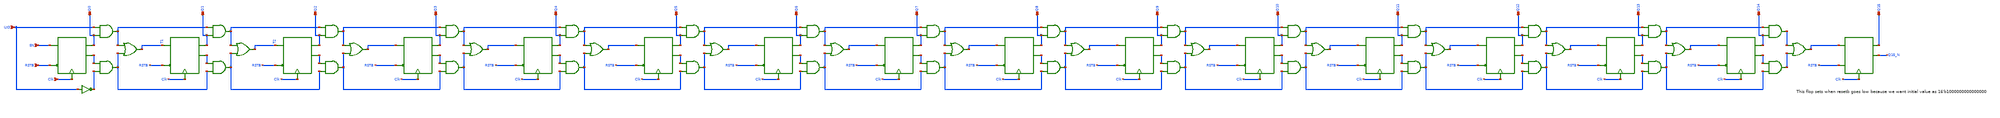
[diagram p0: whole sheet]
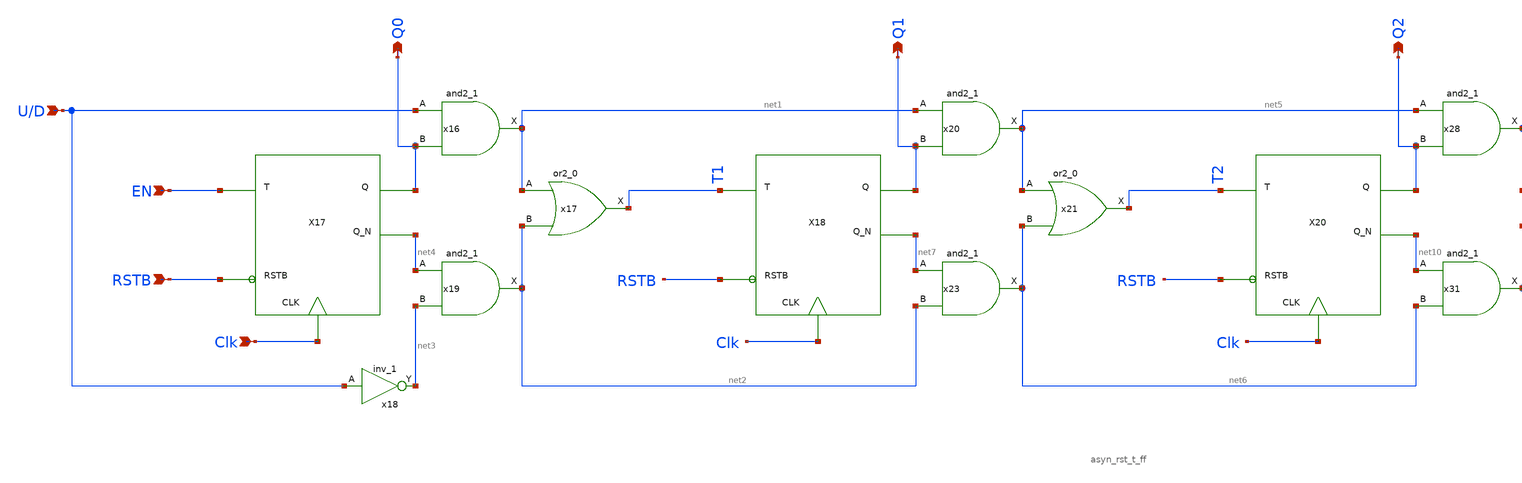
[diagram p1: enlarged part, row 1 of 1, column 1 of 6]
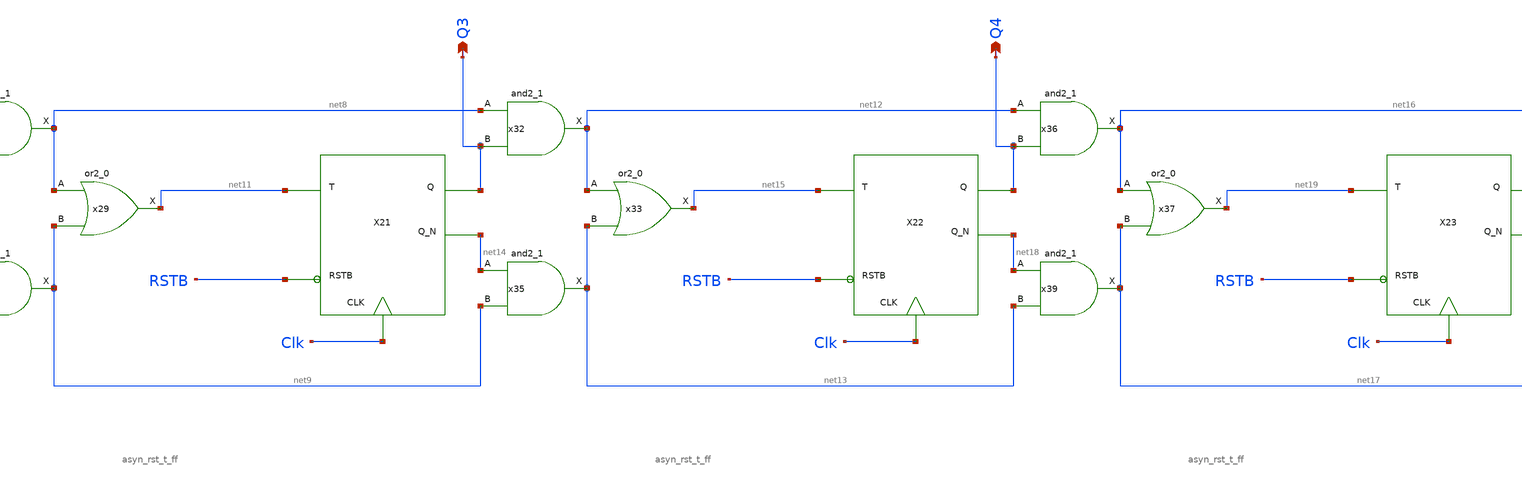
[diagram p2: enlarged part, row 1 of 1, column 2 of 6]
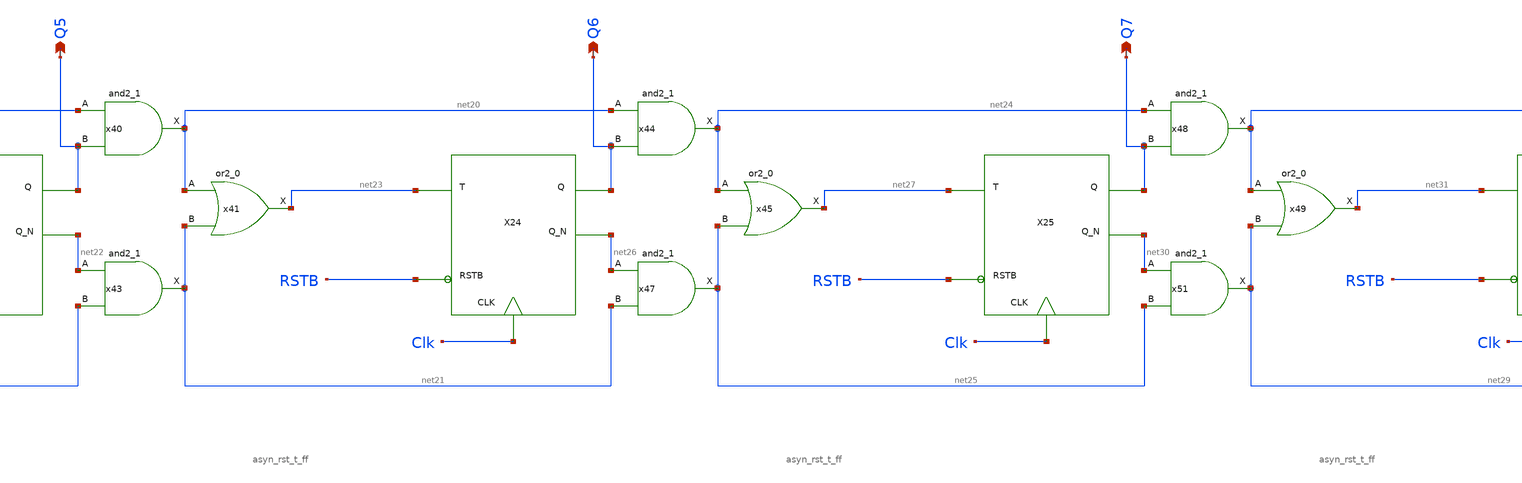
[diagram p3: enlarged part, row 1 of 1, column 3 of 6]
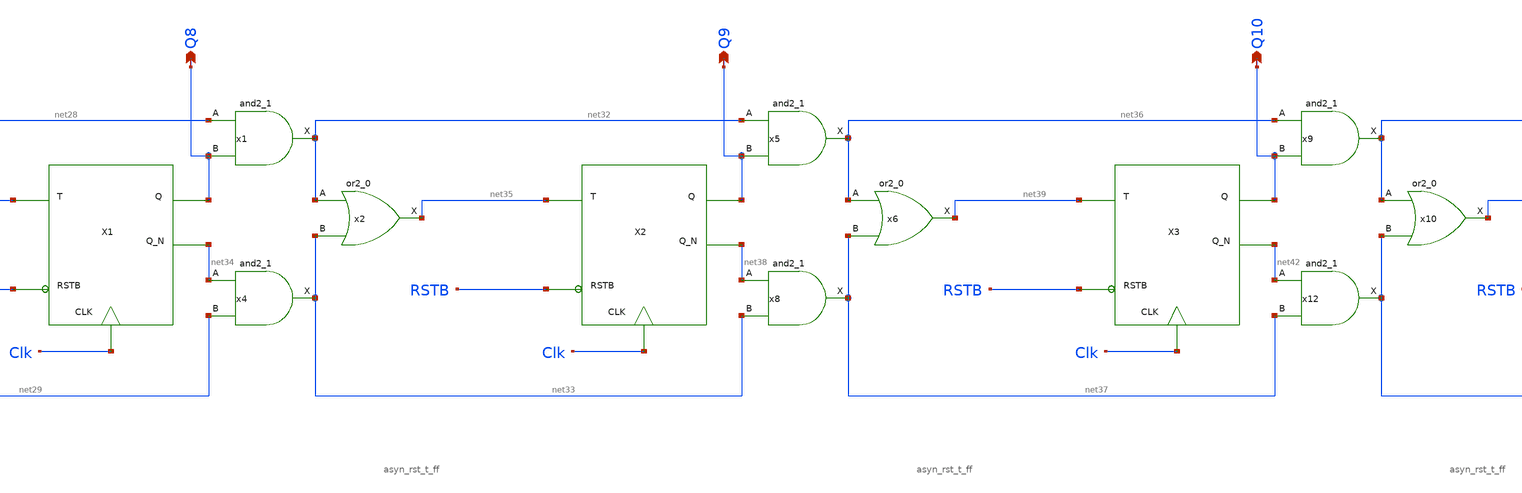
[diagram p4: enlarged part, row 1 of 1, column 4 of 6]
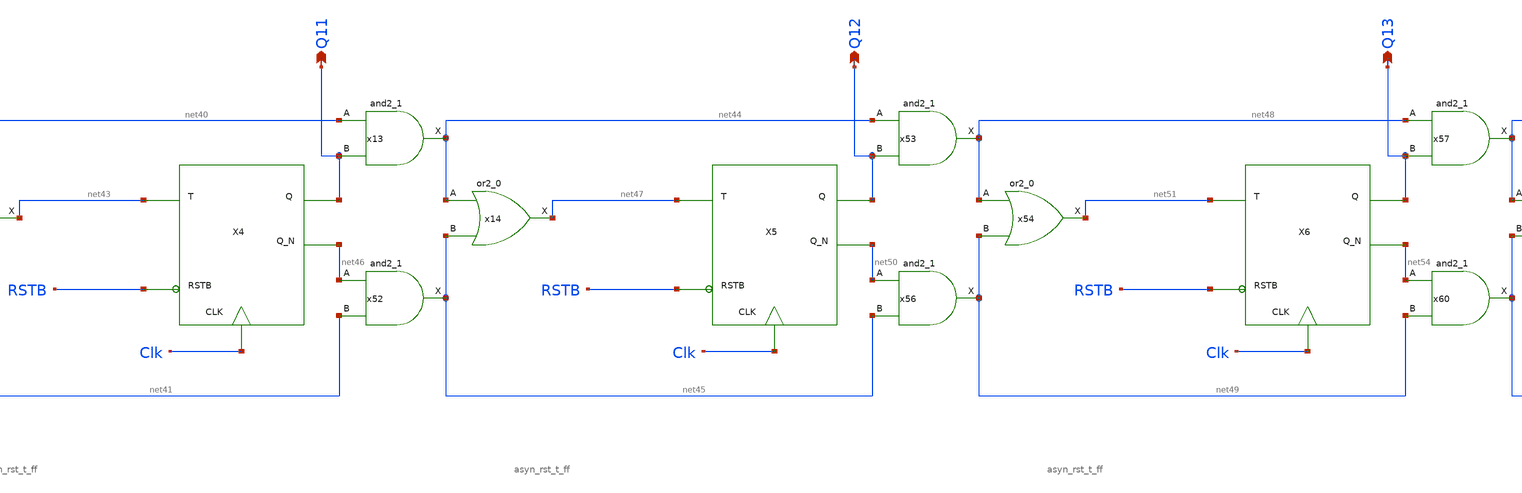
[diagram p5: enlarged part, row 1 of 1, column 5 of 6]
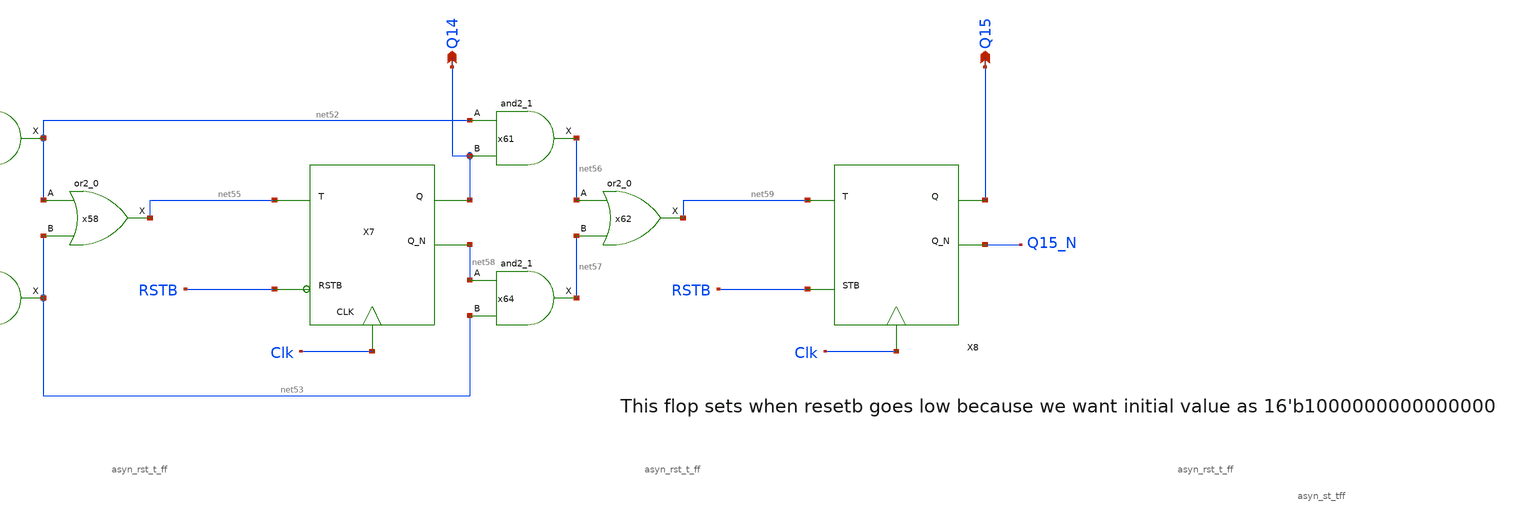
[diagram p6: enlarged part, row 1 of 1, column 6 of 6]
** sch_path: xschem/binary counter/bin_counter.sch
**.subckt bin_counter Clk EN Q0 RSTB U/D Q1 Q2 Q3 Q4 Q5 Q6 Q7 Q8 Q9 Q10 Q11 Q12 Q13 Q14 Q15
*.ipin Clk
*.ipin EN
*.opin Q0
*.ipin RSTB
*.ipin U/D
*.opin Q1
*.opin Q2
*.opin Q3
*.opin Q4
*.opin Q5
*.opin Q6
*.opin Q7
*.opin Q8
*.opin Q9
*.opin Q10
*.opin Q11
*.opin Q12
*.opin Q13
*.opin Q14
*.opin Q15
x16 U/D Q0 GND GND VDD VDD net1 sky130_fd_sc_lp__and2_1
X17 EN Q0 Clk RSTB net4 asyn_rst_t_ff
x17 net1 net2 GND GND VDD VDD T1 sky130_fd_sc_lp__or2_0
x18 U/D GND GND VDD VDD net3 sky130_fd_sc_lp__inv_1
x19 net4 net3 GND GND VDD VDD net2 sky130_fd_sc_lp__and2_1
x20 net1 Q1 GND GND VDD VDD net5 sky130_fd_sc_lp__and2_1
X18 T1 Q1 Clk RSTB net7 asyn_rst_t_ff
x21 net5 net6 GND GND VDD VDD T2 sky130_fd_sc_lp__or2_0
x23 net7 net2 GND GND VDD VDD net6 sky130_fd_sc_lp__and2_1
x28 net5 Q2 GND GND VDD VDD net8 sky130_fd_sc_lp__and2_1
X20 T2 Q2 Clk RSTB net10 asyn_rst_t_ff
x29 net8 net9 GND GND VDD VDD net11 sky130_fd_sc_lp__or2_0
x31 net10 net6 GND GND VDD VDD net9 sky130_fd_sc_lp__and2_1
x32 net8 Q3 GND GND VDD VDD net12 sky130_fd_sc_lp__and2_1
X21 net11 Q3 Clk RSTB net14 asyn_rst_t_ff
x33 net12 net13 GND GND VDD VDD net15 sky130_fd_sc_lp__or2_0
x35 net14 net9 GND GND VDD VDD net13 sky130_fd_sc_lp__and2_1
x36 net12 Q4 GND GND VDD VDD net16 sky130_fd_sc_lp__and2_1
X22 net15 Q4 Clk RSTB net18 asyn_rst_t_ff
x37 net16 net17 GND GND VDD VDD net19 sky130_fd_sc_lp__or2_0
x39 net18 net13 GND GND VDD VDD net17 sky130_fd_sc_lp__and2_1
x40 net16 Q5 GND GND VDD VDD net20 sky130_fd_sc_lp__and2_1
X23 net19 Q5 Clk RSTB net22 asyn_rst_t_ff
x41 net20 net21 GND GND VDD VDD net23 sky130_fd_sc_lp__or2_0
x43 net22 net17 GND GND VDD VDD net21 sky130_fd_sc_lp__and2_1
x44 net20 Q6 GND GND VDD VDD net24 sky130_fd_sc_lp__and2_1
X24 net23 Q6 Clk RSTB net26 asyn_rst_t_ff
x45 net24 net25 GND GND VDD VDD net27 sky130_fd_sc_lp__or2_0
x47 net26 net21 GND GND VDD VDD net25 sky130_fd_sc_lp__and2_1
x48 net24 Q7 GND GND VDD VDD net28 sky130_fd_sc_lp__and2_1
X25 net27 Q7 Clk RSTB net30 asyn_rst_t_ff
x49 net28 net29 GND GND VDD VDD net31 sky130_fd_sc_lp__or2_0
x51 net30 net25 GND GND VDD VDD net29 sky130_fd_sc_lp__and2_1
x1 net28 Q8 GND GND VDD VDD net32 sky130_fd_sc_lp__and2_1
X1 net31 Q8 Clk RSTB net34 asyn_rst_t_ff
x2 net32 net33 GND GND VDD VDD net35 sky130_fd_sc_lp__or2_0
x4 net34 net29 GND GND VDD VDD net33 sky130_fd_sc_lp__and2_1
x5 net32 Q9 GND GND VDD VDD net36 sky130_fd_sc_lp__and2_1
X2 net35 Q9 Clk RSTB net38 asyn_rst_t_ff
x6 net36 net37 GND GND VDD VDD net39 sky130_fd_sc_lp__or2_0
x8 net38 net33 GND GND VDD VDD net37 sky130_fd_sc_lp__and2_1
x9 net36 Q10 GND GND VDD VDD net40 sky130_fd_sc_lp__and2_1
X3 net39 Q10 Clk RSTB net42 asyn_rst_t_ff
x10 net40 net41 GND GND VDD VDD net43 sky130_fd_sc_lp__or2_0
x12 net42 net37 GND GND VDD VDD net41 sky130_fd_sc_lp__and2_1
x13 net40 Q11 GND GND VDD VDD net44 sky130_fd_sc_lp__and2_1
X4 net43 Q11 Clk RSTB net46 asyn_rst_t_ff
x14 net44 net45 GND GND VDD VDD net47 sky130_fd_sc_lp__or2_0
x52 net46 net41 GND GND VDD VDD net45 sky130_fd_sc_lp__and2_1
x53 net44 Q12 GND GND VDD VDD net48 sky130_fd_sc_lp__and2_1
X5 net47 Q12 Clk RSTB net50 asyn_rst_t_ff
x54 net48 net49 GND GND VDD VDD net51 sky130_fd_sc_lp__or2_0
x56 net50 net45 GND GND VDD VDD net49 sky130_fd_sc_lp__and2_1
x57 net48 Q13 GND GND VDD VDD net52 sky130_fd_sc_lp__and2_1
X6 net51 Q13 Clk RSTB net54 asyn_rst_t_ff
x58 net52 net53 GND GND VDD VDD net55 sky130_fd_sc_lp__or2_0
x60 net54 net49 GND GND VDD VDD net53 sky130_fd_sc_lp__and2_1
x61 net52 Q14 GND GND VDD VDD net56 sky130_fd_sc_lp__and2_1
X7 net55 Q14 Clk RSTB net58 asyn_rst_t_ff
x62 net56 net57 GND GND VDD VDD net59 sky130_fd_sc_lp__or2_0
x64 net58 net53 GND GND VDD VDD net57 sky130_fd_sc_lp__and2_1
X8 net59 RSTB Q15 Q15_N Clk asyn_st_tff
**.ends

* expanding   symbol:  T_flip_flop/asyn_rst_t_ff.sym # of pins=5
** sym_path: xschem/T_flip_flop/asyn_rst_t_ff.sym
** sch_path: xschem/T_flip_flop/asyn_rst_t_ff.sch
.subckt asyn_rst_t_ff T Q CLK RSTB Q_N
*.ipin T
*.ipin CLK
*.opin Q
*.ipin RSTB
*.opin Q_N
x3 T Q GND GND VDD VDD net1 sky130_fd_sc_lp__xor2_1
x2 Q GND GND VDD VDD Q_N sky130_fd_sc_lp__inv_1
x1 CLK net1 RSTB GND GND VDD VDD Q sky130_fd_sc_lp__dfrtp_1
.ends


* expanding   symbol:  T_flip_flop/asyn_st_tff.sym # of pins=5
** sym_path: xschem/T_flip_flop/asyn_st_tff.sym
** sch_path: xschem/T_flip_flop/asyn_st_tff.sch
.subckt asyn_st_tff T STB Q Q_N CLK
*.ipin T
*.ipin CLK
*.opin Q
*.ipin STB
*.opin Q_N
x3 T Q GND GND VDD VDD net1 sky130_fd_sc_lp__xor2_1
x1 CLK net1 STB GND GND VDD VDD Q Q_N sky130_fd_sc_lp__dfsbp_1
.ends

.end
